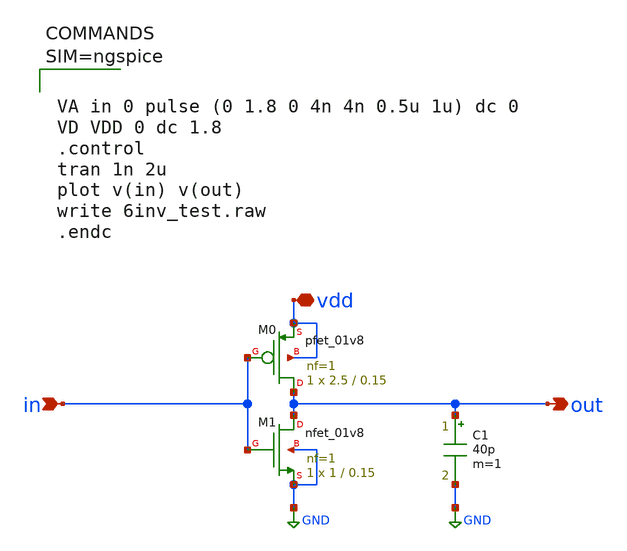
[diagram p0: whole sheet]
** sch_path: inv_drive.sch
**.subckt inv_drive in vdd out
*.ipin in
*.iopin vdd
*.opin out
XM1 out in GND GND sky130_fd_pr__nfet_01v8 L=0.15 W=1 nf=1 ad='int((nf+1)/2) * W/nf * 0.29' as='int((nf+2)/2) * W/nf * 0.29'
+ pd='2*int((nf+1)/2) * (W/nf + 0.29)' ps='2*int((nf+2)/2) * (W/nf + 0.29)' nrd='0.29 / W' nrs='0.29 / W'
+ sa=0 sb=0 sd=0 mult=1 m=1
XM0 out in vdd vdd sky130_fd_pr__pfet_01v8 L=0.15 W=2.5 nf=1 ad='int((nf+1)/2) * W/nf * 0.29' as='int((nf+2)/2) * W/nf * 0.29'
+ pd='2*int((nf+1)/2) * (W/nf + 0.29)' ps='2*int((nf+2)/2) * (W/nf + 0.29)' nrd='0.29 / W' nrs='0.29 / W'
+ sa=0 sb=0 sd=0 mult=1 m=1
C1 out GND 40p m=1
**** begin user architecture code



VA in 0 pulse (0 1.8 0 4n 4n 0.5u 1u) dc 0
VD VDD 0 dc 1.8
.control
tran 1n 2u
plot v(in) v(out)
write 6inv_test.raw
.endc




** opencircuitdesign pdks install
.lib $::SKYWATER_MODELS/sky130.lib.spice ss


**** end user architecture code
**.ends
.GLOBAL GND
.end
